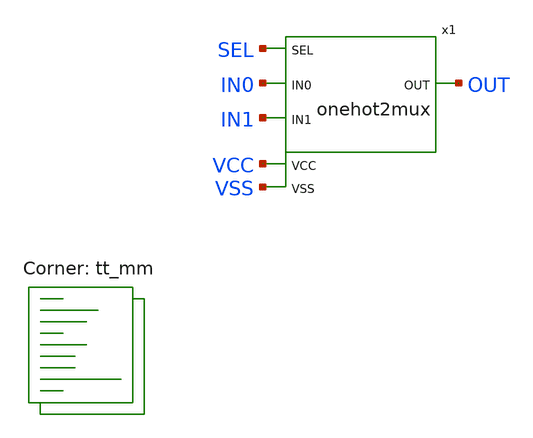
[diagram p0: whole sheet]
** sch_path: xschem/tb_onehot2mux.sch
* StefanSchippers/xschem_sky130/sky130_tests/lvtnot.sch:
* Copyright 2020 Stefan Frederik Schippers
* Licensed under the Apache License, Version 2.0 (the "License");
**.subckt tb_onehot2mux
x1 VCC VSS SEL IN1 OUT IN0 onehot2mux
**** begin user architecture code
.lib $::SKYWATER_MODELS/sky130.lib.spice tt_mm


** this experimental option enables mos model bin
** selection based on W/NF instead of W
.option chgtol=4e-16 method=gear

.param VCCGAUSS = agauss(1.8, 0.05, 1)
.param VCC = 'VCCGAUSS'
** use following line to remove VCC variations
* .param VCC = 1.8
.param VDLGAUSS = agauss(0.9, 0.23, 1)
.param VDL = VDLGAUSS
** use following line to remove input common mode variations
* .param VDL =  0.9
.param TEMPGAUSS = agauss(40, 30, 1)
.option temp = 'TEMPGAUSS'
** use following line to remove temperature variations
* .option temp = 25
.param DELTA = 0.002

.include stimuli_tb_onehot2mux.cir

.control
  setseed  8
  reset
  let run = 1
  save all
  op
  write tb_onehot2mux.raw
  reset
  set appendwrite
  dowhile run < = 5
    save all
    tran 1n 1000n uic
    write tb_onehot2mux.raw
    let run = run + 1
    reset
  end
  quit 0
.endc


**** end user architecture code
**.ends

* expanding   symbol:  /home/ttuser/wowa/xschem/onehot2mux.sym # of pins=6
** sym_path: /home/ttuser/wowa/xschem/onehot2mux.sym
** sch_path: /home/ttuser/wowa/xschem/onehot2mux.sch
.subckt onehot2mux VCC VSS SEL IN1 OUT IN0
*.ipin SEL
*.ipin IN0
*.ipin IN1
*.opin OUT
*.ipin VCC
*.ipin VSS
x1 OUT IN1 SEL_N SEL VCC VSS passgate W_N=2 L_N=0.2 W_P=2 L_P=0.2 m=2
x3 OUT IN0 SEL SEL_N VCC VSS passgate W_N=2 L_N=0.2 W_P=2 L_P=0.2 m=2
x5 SEL SEL_N VCC VSS lvtnot W_N=1 L_N=0.15 W_P=2 L_P=0.35 m=1
.ends


* expanding   symbol:  sky130_tests/passgate.sym # of pins=4
** sym_path: sky130_tests/passgate.sym
** sch_path: sky130_tests/passgate.sch
.subckt passgate Z A GP GN VCCBPIN VSSBPIN  W_N=1 L_N=0.2 W_P=1 L_P=0.2

*.iopin A
*.iopin Z
*.ipin GP
*.ipin GN
XM1 A GN Z VSS sky130_fd_pr__nfet_01v8 W=W_N L=L_N ad='W * 0.29' pd='W + 2 * 0.29' as='W * 0.29' ps='W + 2 * 0.29'
+ nrd=0 nrs=0 sa=0 sb=0 sd=0 nf=1 mult=1
XM2 A GP Z VCC sky130_fd_pr__pfet_01v8 W=W_P L=L_P ad='W * 0.29' pd='W + 2 * 0.29' as='W * 0.29' ps='W + 2 * 0.29'
+ nrd=0 nrs=0 sa=0 sb=0 sd=0 nf=1 mult=1
.ends


* expanding   symbol:  sky130_tests/lvtnot.sym # of pins=2
** sym_path: sky130_tests/lvtnot.sym
** sch_path: sky130_tests/lvtnot.sch
.subckt lvtnot a y VCCPIN VSSPIN     W_N=1 L_N=0.15 W_P=2 L_P=0.35
*.opin y
*.ipin a
XM1 y a VSSPIN VSSPIN sky130_fd_pr__nfet_01v8_lvt L=L_N W=W_N nf=1 ad='int((1 + 1)/2) * W_N / 1 * 0.29'
+ as='int((1 + 2)/2) * W_N / 1 * 0.29' pd='2*int((1 + 1)/2) * (W_N / 1 + 0.29)' ps='2*int((1 + 2)/2) * (W_N / 1 + 0.29)'
+ nrd='0.29 / W_N ' nrs='0.29 / W_N ' sa=0 sb=0 sd=0 mult=1 m=1
XM2 y a VCCPIN VCCPIN sky130_fd_pr__pfet_01v8_lvt L=L_P W=W_P nf=1 ad='int((1 + 1)/2) * W_P / 1 * 0.29'
+ as='int((1 + 2)/2) * W_P / 1 * 0.29' pd='2*int((1 + 1)/2) * (W_P / 1 + 0.29)' ps='2*int((1 + 2)/2) * (W_P / 1 + 0.29)'
+ nrd='0.29 / W_P ' nrs='0.29 / W_P ' sa=0 sb=0 sd=0 mult=1 m=1
.ends

.end
